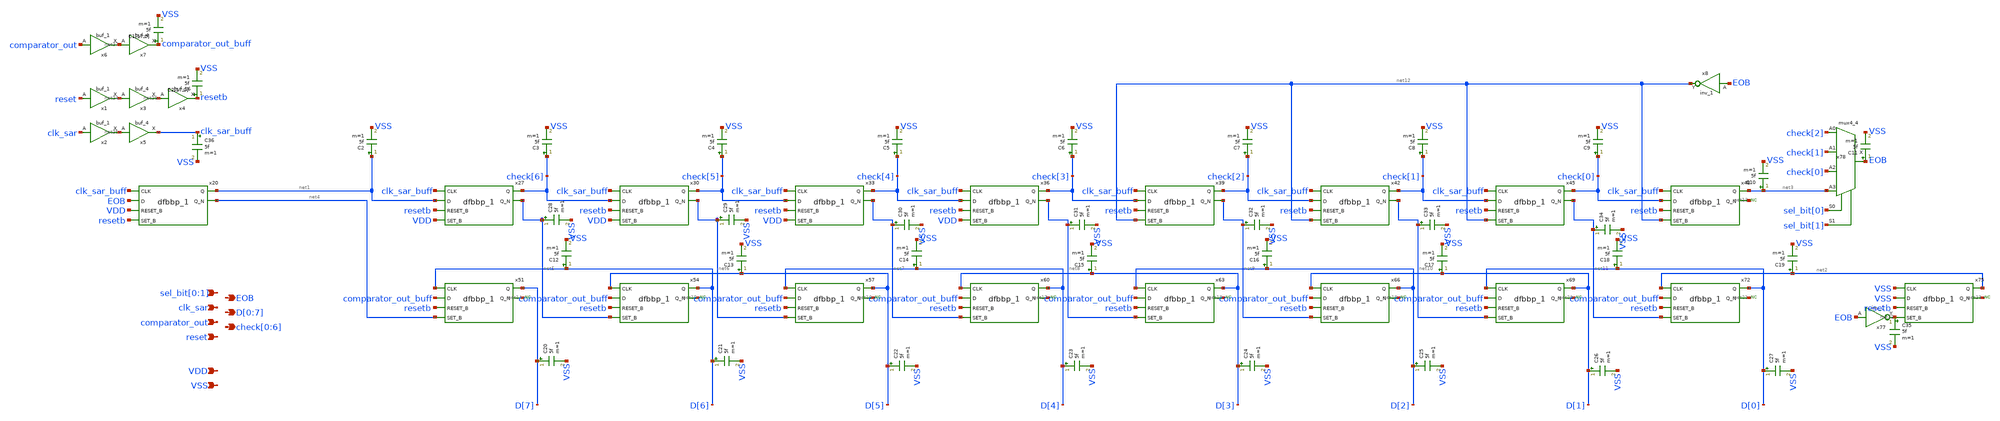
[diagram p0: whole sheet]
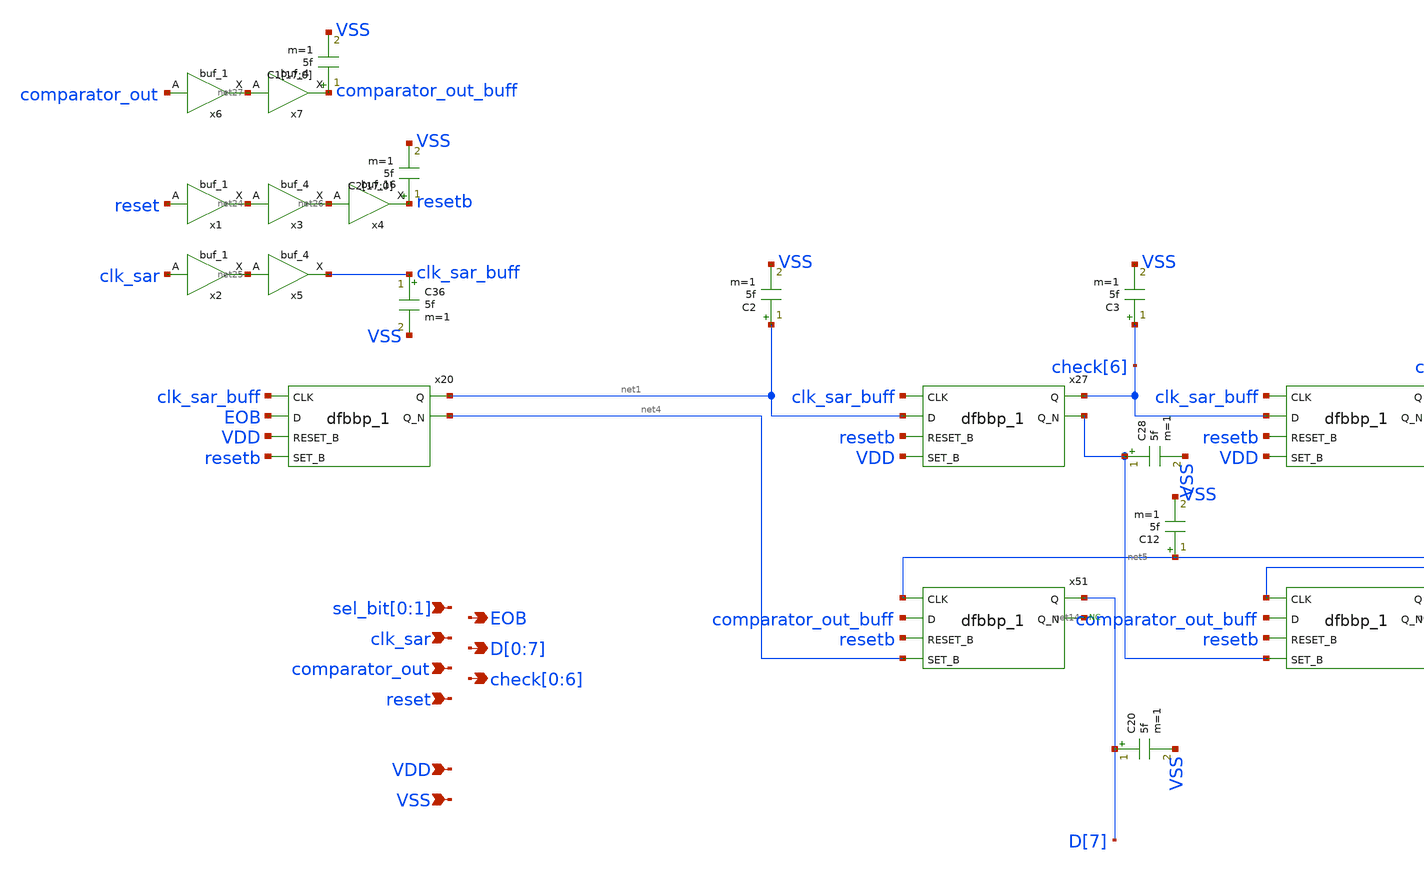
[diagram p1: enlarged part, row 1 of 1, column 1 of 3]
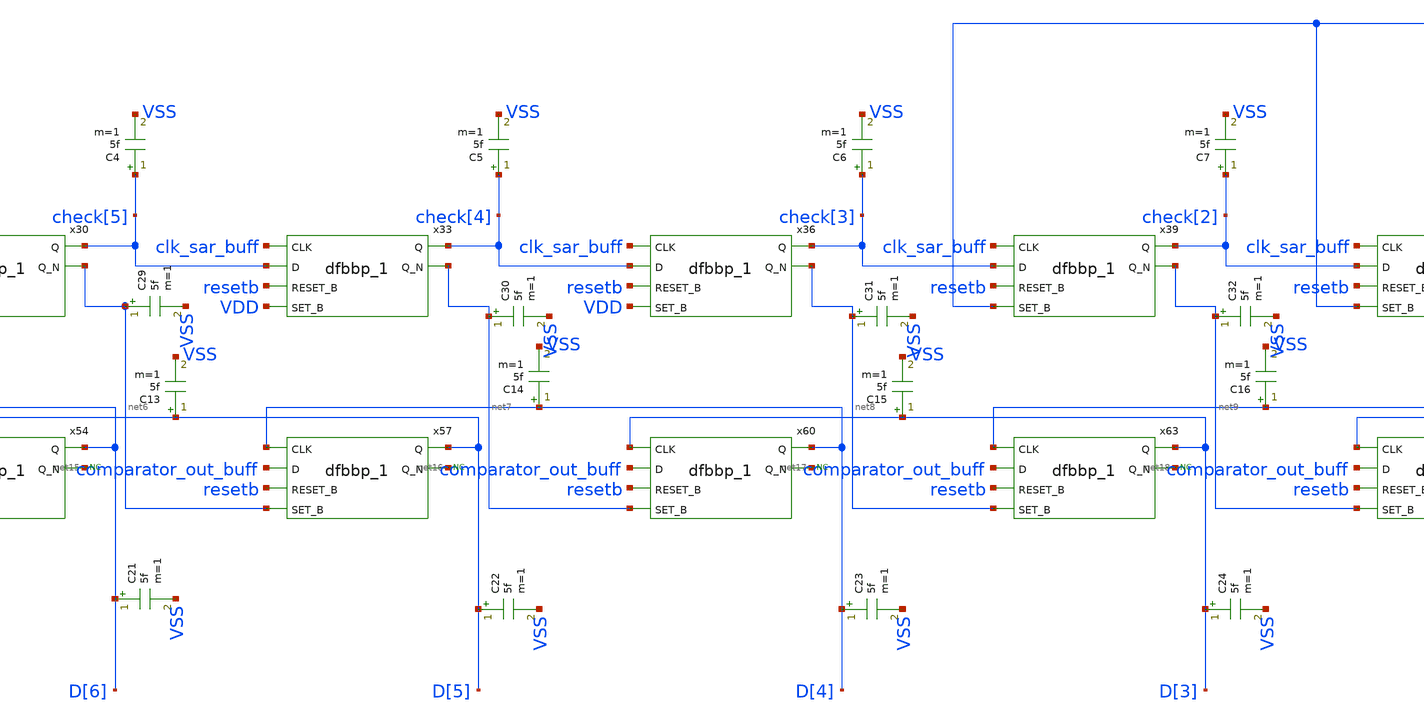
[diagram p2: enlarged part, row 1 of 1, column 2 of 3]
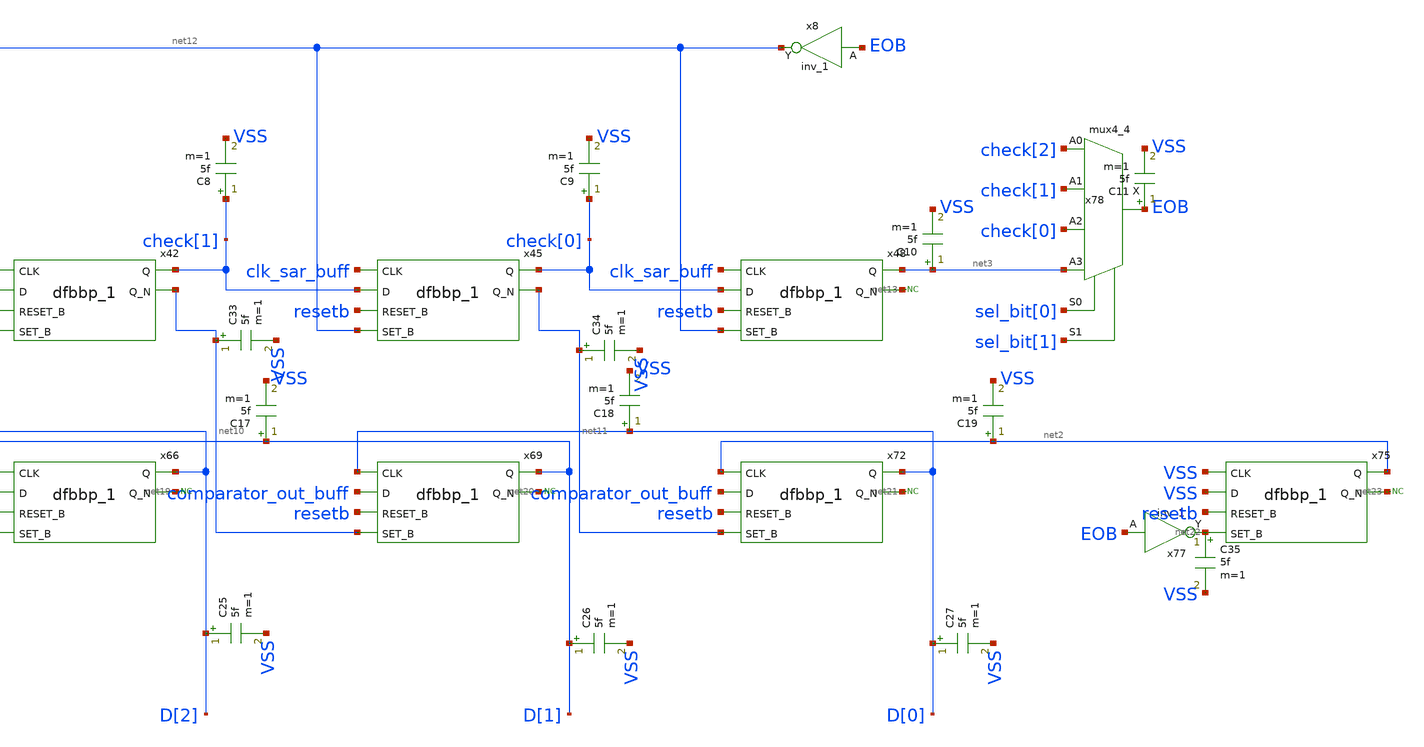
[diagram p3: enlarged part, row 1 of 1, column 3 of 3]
** sch_path: hgu/xschem/hgu_sarlogic_8bit_logic_LPW.sch
**.subckt hgu_sarlogic_8bit_logic_LPW clk_sar VDD VSS comparator_out reset EOB
*+ D[0],D[1],D[2],D[3],D[4],D[5],D[6],D[7] check[0],check[1],check[2],check[3],check[4],check[5],check[6] sel_bit[0],sel_bit[1]
*.ipin clk_sar
*.ipin VDD
*.ipin VSS
*.ipin comparator_out
*.ipin reset
*.opin EOB
*.opin D[0],D[1],D[2],D[3],D[4],D[5],D[6],D[7]
*.opin check[0],check[1],check[2],check[3],check[4],check[5],check[6]
*.ipin sel_bit[0],sel_bit[1]
x20 clk_sar_buff EOB VDD resetb VSS VSS VDD VDD net1 net4 sky130_fd_sc_hd__dfbbp_1
x27 clk_sar_buff net1 resetb VDD VSS VSS VDD VDD check[6] net5 sky130_fd_sc_hd__dfbbp_1
x30 clk_sar_buff check[6] resetb VDD VSS VSS VDD VDD check[5] net6 sky130_fd_sc_hd__dfbbp_1
x33 clk_sar_buff check[5] resetb VDD VSS VSS VDD VDD check[4] net7 sky130_fd_sc_hd__dfbbp_1
x36 clk_sar_buff check[4] resetb VDD VSS VSS VDD VDD check[3] net8 sky130_fd_sc_hd__dfbbp_1
x39 clk_sar_buff check[3] resetb net12 VSS VSS VDD VDD check[2] net9 sky130_fd_sc_hd__dfbbp_1
x42 clk_sar_buff check[2] resetb net12 VSS VSS VDD VDD check[1] net10 sky130_fd_sc_hd__dfbbp_1
x45 clk_sar_buff check[1] resetb net12 VSS VSS VDD VDD check[0] net11 sky130_fd_sc_hd__dfbbp_1
x48 clk_sar_buff check[0] resetb net12 VSS VSS VDD VDD net3 net13 sky130_fd_sc_hd__dfbbp_1
x51 D[6] comparator_out_buff resetb net4 VSS VSS VDD VDD D[7] net14 sky130_fd_sc_hd__dfbbp_1
x54 D[5] comparator_out_buff resetb net5 VSS VSS VDD VDD D[6] net15 sky130_fd_sc_hd__dfbbp_1
x57 D[4] comparator_out_buff resetb net6 VSS VSS VDD VDD D[5] net16 sky130_fd_sc_hd__dfbbp_1
x60 D[3] comparator_out_buff resetb net7 VSS VSS VDD VDD D[4] net17 sky130_fd_sc_hd__dfbbp_1
x63 D[2] comparator_out_buff resetb net8 VSS VSS VDD VDD D[3] net18 sky130_fd_sc_hd__dfbbp_1
x66 D[1] comparator_out_buff resetb net9 VSS VSS VDD VDD D[2] net19 sky130_fd_sc_hd__dfbbp_1
x69 D[0] comparator_out_buff resetb net10 VSS VSS VDD VDD D[1] net20 sky130_fd_sc_hd__dfbbp_1
x72 net2 comparator_out_buff resetb net11 VSS VSS VDD VDD D[0] net21 sky130_fd_sc_hd__dfbbp_1
x75 VSS VSS resetb net22 VSS VSS VDD VDD net2 net23 sky130_fd_sc_hd__dfbbp_1
x77 EOB VSS VSS VDD VDD net22 sky130_fd_sc_hd__inv_1
* noconn #net23
x78 check[2] check[1] check[0] net3 sel_bit[0] sel_bit[1] VSS VSS VDD VDD EOB
+ sky130_fd_sc_hd__mux4_4
* noconn #net13
C2[17] resetb VSS 5f m=1
C2[16] resetb VSS 5f m=1
C2[15] resetb VSS 5f m=1
C2[14] resetb VSS 5f m=1
C2[13] resetb VSS 5f m=1
C2[12] resetb VSS 5f m=1
C2[11] resetb VSS 5f m=1
C2[10] resetb VSS 5f m=1
C2[9] resetb VSS 5f m=1
C2[8] resetb VSS 5f m=1
C2[7] resetb VSS 5f m=1
C2[6] resetb VSS 5f m=1
C2[5] resetb VSS 5f m=1
C2[4] resetb VSS 5f m=1
C2[3] resetb VSS 5f m=1
C2[2] resetb VSS 5f m=1
C2[1] resetb VSS 5f m=1
C2[0] resetb VSS 5f m=1
C2 net1 VSS 5f m=1
C3 check[6] VSS 5f m=1
C4 check[5] VSS 5f m=1
C5 check[4] VSS 5f m=1
C6 check[3] VSS 5f m=1
C7 check[2] VSS 5f m=1
C8 check[1] VSS 5f m=1
C9 check[0] VSS 5f m=1
C10 net3 VSS 5f m=1
C11 EOB VSS 5f m=1
C12 D[6] VSS 5f m=1
C13 D[5] VSS 5f m=1
C14 D[4] VSS 5f m=1
C15 D[3] VSS 5f m=1
C16 D[2] VSS 5f m=1
C17 D[1] VSS 5f m=1
C18 D[0] VSS 5f m=1
C19 net2 VSS 5f m=1
C20 D[7] VSS 5f m=1
C21 D[6] VSS 5f m=1
C22 D[5] VSS 5f m=1
C23 D[4] VSS 5f m=1
C24 D[3] VSS 5f m=1
C25 D[2] VSS 5f m=1
C26 D[1] VSS 5f m=1
C27 D[0] VSS 5f m=1
C28 net5 VSS 5f m=1
C29 net6 VSS 5f m=1
C30 net7 VSS 5f m=1
C31 net8 VSS 5f m=1
C32 net9 VSS 5f m=1
C33 net10 VSS 5f m=1
C34 net11 VSS 5f m=1
C35 net22 VSS 5f m=1
C36 clk_sar_buff VSS 5f m=1
x1 reset VSS VSS VDD VDD net24 sky130_fd_sc_hd__buf_1
x2 clk_sar VSS VSS VDD VDD net25 sky130_fd_sc_hd__buf_1
x3 net24 VSS VSS VDD VDD net26 sky130_fd_sc_hd__buf_4
x4 net26 VSS VSS VDD VDD resetb sky130_fd_sc_hd__buf_16
* noconn #net21
* noconn #net20
* noconn #net19
* noconn #net18
* noconn #net17
* noconn #net16
* noconn #net15
* noconn #net14
x5 net25 VSS VSS VDD VDD clk_sar_buff sky130_fd_sc_hd__buf_4
x6 comparator_out VSS VSS VDD VDD net27 sky130_fd_sc_hd__buf_1
x7 net27 VSS VSS VDD VDD comparator_out_buff sky130_fd_sc_hd__buf_4
C1[17] comparator_out_buff VSS 5f m=1
C1[16] comparator_out_buff VSS 5f m=1
C1[15] comparator_out_buff VSS 5f m=1
C1[14] comparator_out_buff VSS 5f m=1
C1[13] comparator_out_buff VSS 5f m=1
C1[12] comparator_out_buff VSS 5f m=1
C1[11] comparator_out_buff VSS 5f m=1
C1[10] comparator_out_buff VSS 5f m=1
C1[9] comparator_out_buff VSS 5f m=1
C1[8] comparator_out_buff VSS 5f m=1
C1[7] comparator_out_buff VSS 5f m=1
C1[6] comparator_out_buff VSS 5f m=1
C1[5] comparator_out_buff VSS 5f m=1
C1[4] comparator_out_buff VSS 5f m=1
C1[3] comparator_out_buff VSS 5f m=1
C1[2] comparator_out_buff VSS 5f m=1
C1[1] comparator_out_buff VSS 5f m=1
C1[0] comparator_out_buff VSS 5f m=1
x8 EOB VSS VSS vDD VDD net12 sky130_fd_sc_hd__inv_1
**.ends
.end
